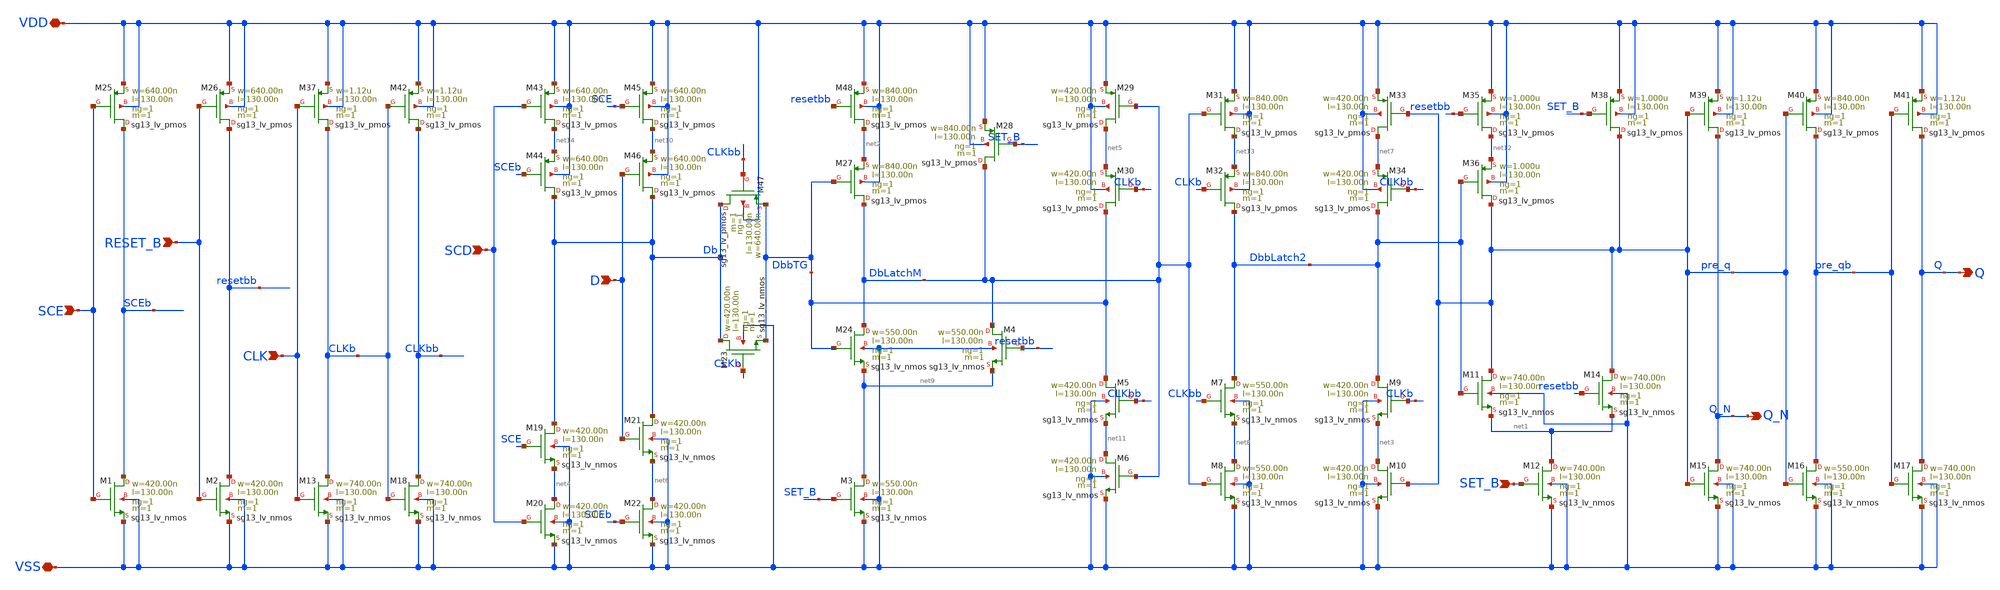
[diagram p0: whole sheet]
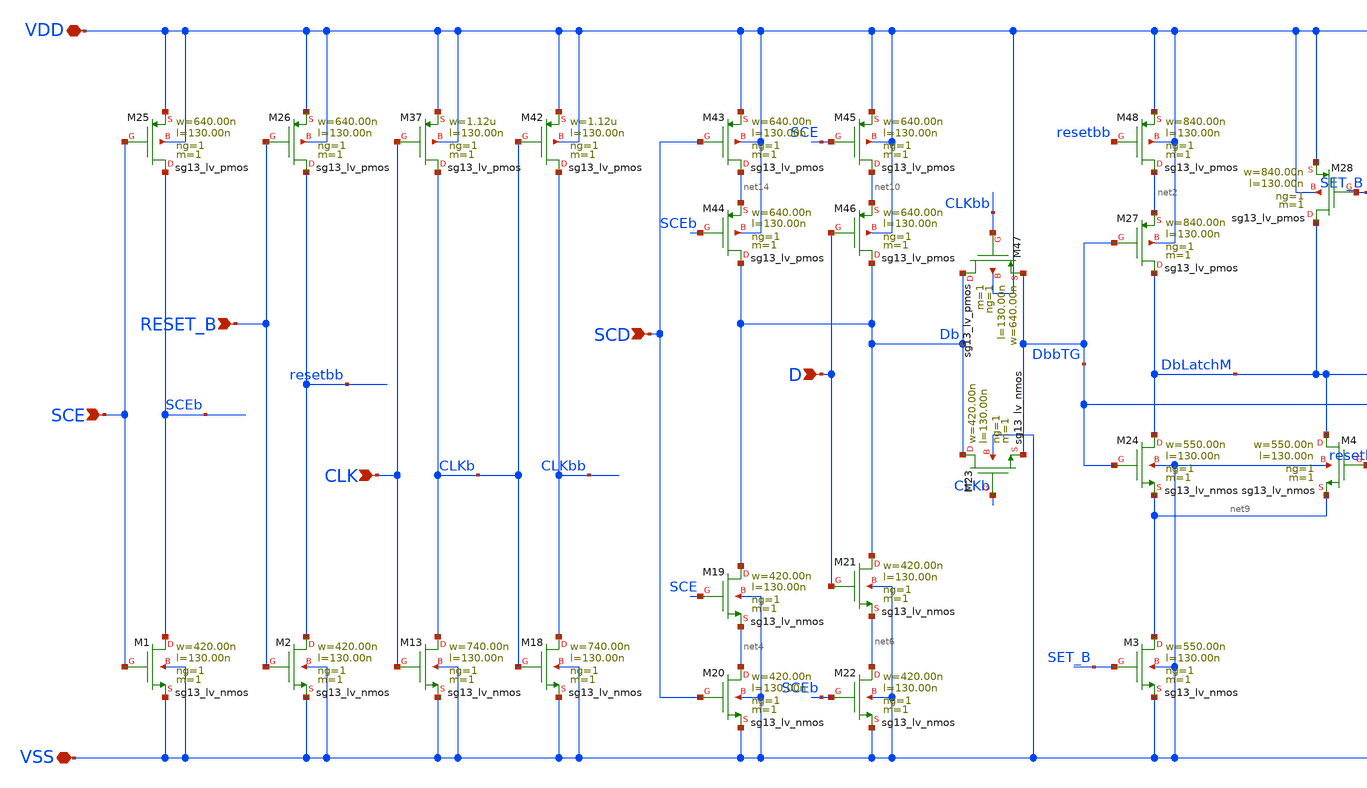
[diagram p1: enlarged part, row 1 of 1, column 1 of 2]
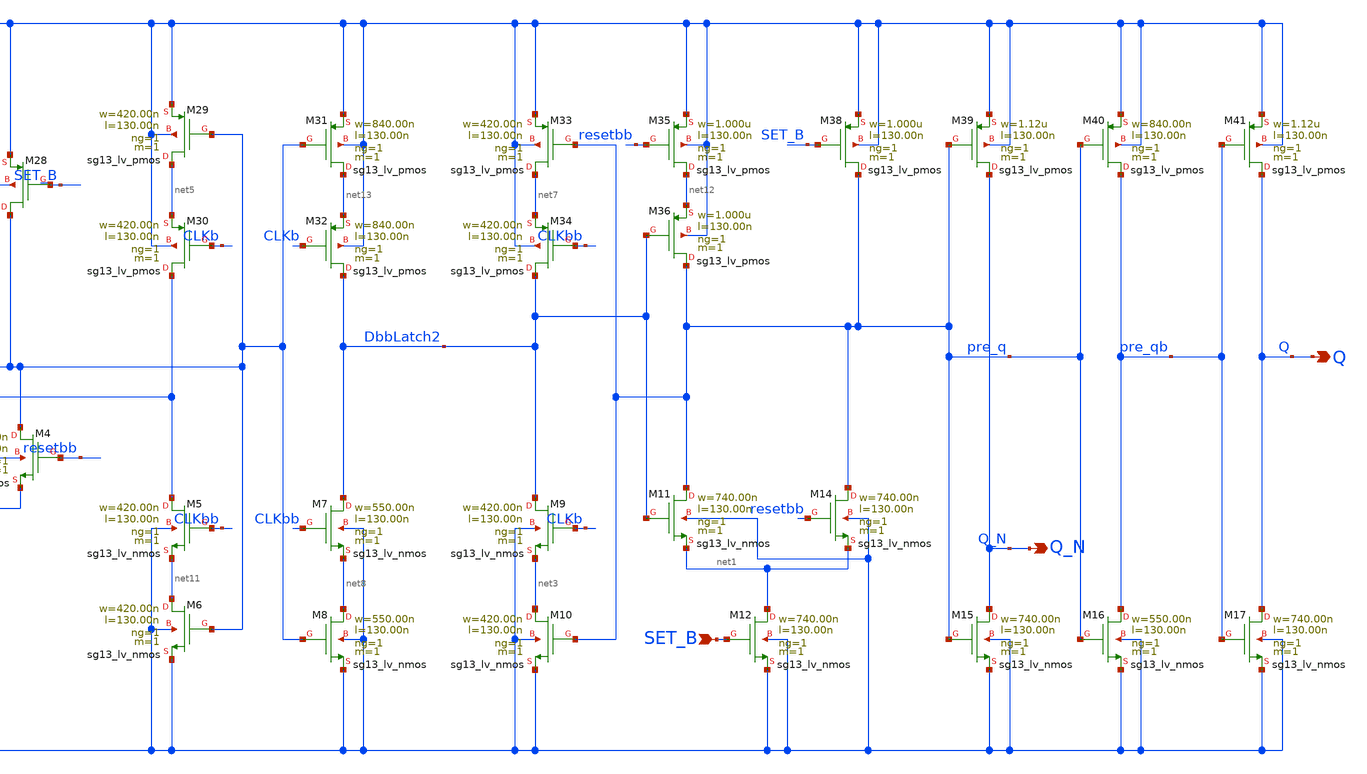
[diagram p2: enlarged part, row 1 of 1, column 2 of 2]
** sch_path: ihp-sg13g2/libs.tech/xschem/sg13g2_stdcells/sg13g2_sdfbbp_1.sch
**.subckt sg13g2_sdfbbp_1 Q_N Q SCD VDD VSS SET_B SCE RESET_B D CLK
*.opin Q_N
*.opin Q
*.ipin SCD
*.iopin VDD
*.iopin VSS
*.ipin SET_B
*.ipin SCE
*.ipin RESET_B
*.ipin D
*.ipin CLK
XM1 SCEb SCE VSS VSS sg13_lv_nmos w=420.00n l=130.00n ng=1 m=1 mm_ok=1
XM2 resetbb RESET_B VSS VSS sg13_lv_nmos w=420.00n l=130.00n ng=1 m=1 mm_ok=1
XM3 net9 SET_B VSS VSS sg13_lv_nmos w=550.00n l=130.00n ng=1 m=1 mm_ok=1
XM4 DbLatchM resetbb net9 VSS sg13_lv_nmos w=550.00n l=130.00n ng=1 m=1 mm_ok=1
XM5 DbbTG CLKbb net11 VSS sg13_lv_nmos w=420.00n l=130.00n ng=1 m=1 mm_ok=1
XM6 net11 DbLatchM VSS VSS sg13_lv_nmos w=420.00n l=130.00n ng=1 m=1 mm_ok=1
XM7 DbbLatch2 CLKbb net8 VSS sg13_lv_nmos w=550.00n l=130.00n ng=1 m=1 mm_ok=1
XM8 net8 DbLatchM VSS VSS sg13_lv_nmos w=550.00n l=130.00n ng=1 m=1 mm_ok=1
XM9 DbbLatch2 CLKb net3 VSS sg13_lv_nmos w=420.00n l=130.00n ng=1 m=1 mm_ok=1
XM10 net3 pre_q VSS VSS sg13_lv_nmos w=420.00n l=130.00n ng=1 m=1 mm_ok=1
XM11 pre_q DbbLatch2 net1 VSS sg13_lv_nmos w=740.00n l=130.00n ng=1 m=1 mm_ok=1
XM12 net1 SET_B VSS VSS sg13_lv_nmos w=740.00n l=130.00n ng=1 m=1 mm_ok=1
XM13 CLKb CLK VSS VSS sg13_lv_nmos w=740.00n l=130.00n ng=1 m=1 mm_ok=1
XM14 pre_q resetbb net1 VSS sg13_lv_nmos w=740.00n l=130.00n ng=1 m=1 mm_ok=1
XM15 Q_N pre_q VSS VSS sg13_lv_nmos w=740.00n l=130.00n ng=1 m=1 mm_ok=1
XM16 pre_qb pre_q VSS VSS sg13_lv_nmos w=550.00n l=130.00n ng=1 m=1 mm_ok=1
XM17 Q pre_qb VSS VSS sg13_lv_nmos w=740.00n l=130.00n ng=1 m=1 mm_ok=1
XM18 CLKbb CLKb VSS VSS sg13_lv_nmos w=740.00n l=130.00n ng=1 m=1 mm_ok=1
XM19 Db SCE net4 VSS sg13_lv_nmos w=420.00n l=130.00n ng=1 m=1 mm_ok=1
XM20 net4 SCD VSS VSS sg13_lv_nmos w=420.00n l=130.00n ng=1 m=1 mm_ok=1
XM21 Db D net6 VSS sg13_lv_nmos w=420.00n l=130.00n ng=1 m=1 mm_ok=1
XM22 net6 SCEb VSS VSS sg13_lv_nmos w=420.00n l=130.00n ng=1 m=1 mm_ok=1
XM23 Db CLKb DbbTG VSS sg13_lv_nmos w=420.00n l=130.00n ng=1 m=1 mm_ok=1
XM24 DbLatchM DbbTG net9 VSS sg13_lv_nmos w=550.00n l=130.00n ng=1 m=1 mm_ok=1
XM25 SCEb SCE VDD VDD sg13_lv_pmos w=640.00n l=130.00n ng=1 m=1 mm_ok=1
XM26 resetbb RESET_B VDD VDD sg13_lv_pmos w=640.00n l=130.00n ng=1 m=1 mm_ok=1
XM27 DbLatchM DbbTG net2 VDD sg13_lv_pmos w=840.00n l=130.00n ng=1 m=1 mm_ok=1
XM28 DbLatchM SET_B VDD VDD sg13_lv_pmos w=840.00n l=130.00n ng=1 m=1 mm_ok=1
XM29 net5 DbLatchM VDD VDD sg13_lv_pmos w=420.00n l=130.00n ng=1 m=1 mm_ok=1
XM30 DbbTG CLKb net5 VDD sg13_lv_pmos w=420.00n l=130.00n ng=1 m=1 mm_ok=1
XM31 net13 DbLatchM VDD VDD sg13_lv_pmos w=840.00n l=130.00n ng=1 m=1 mm_ok=1
XM32 DbbLatch2 CLKb net13 VDD sg13_lv_pmos w=840.00n l=130.00n ng=1 m=1 mm_ok=1
XM33 net7 pre_q VDD VDD sg13_lv_pmos w=420.00n l=130.00n ng=1 m=1 mm_ok=1
XM34 DbbLatch2 CLKbb net7 VDD sg13_lv_pmos w=420.00n l=130.00n ng=1 m=1 mm_ok=1
XM35 net12 resetbb VDD VDD sg13_lv_pmos w=1.000u l=130.00n ng=1 m=1 mm_ok=1
XM36 pre_q DbbLatch2 net12 VDD sg13_lv_pmos w=1.000u l=130.00n ng=1 m=1 mm_ok=1
XM37 CLKb CLK VDD VDD sg13_lv_pmos w=1.12u l=130.00n ng=1 m=1 mm_ok=1
XM38 pre_q SET_B VDD VDD sg13_lv_pmos w=1.000u l=130.00n ng=1 m=1 mm_ok=1
XM39 Q_N pre_q VDD VDD sg13_lv_pmos w=1.12u l=130.00n ng=1 m=1 mm_ok=1
XM40 pre_qb pre_q VDD VDD sg13_lv_pmos w=840.00n l=130.00n ng=1 m=1 mm_ok=1
XM41 Q pre_qb VDD VDD sg13_lv_pmos w=1.12u l=130.00n ng=1 m=1 mm_ok=1
XM42 CLKbb CLKb VDD VDD sg13_lv_pmos w=1.12u l=130.00n ng=1 m=1 mm_ok=1
XM43 net14 SCD VDD VDD sg13_lv_pmos w=640.00n l=130.00n ng=1 m=1 mm_ok=1
XM44 Db SCEb net14 VDD sg13_lv_pmos w=640.00n l=130.00n ng=1 m=1 mm_ok=1
XM45 net10 SCE VDD VDD sg13_lv_pmos w=640.00n l=130.00n ng=1 m=1 mm_ok=1
XM46 Db D net10 VDD sg13_lv_pmos w=640.00n l=130.00n ng=1 m=1 mm_ok=1
XM47 Db CLKbb DbbTG VDD sg13_lv_pmos w=640.00n l=130.00n ng=1 m=1 mm_ok=1
XM48 net2 resetbb VDD VDD sg13_lv_pmos w=840.00n l=130.00n ng=1 m=1 mm_ok=1
**.ends
.end
